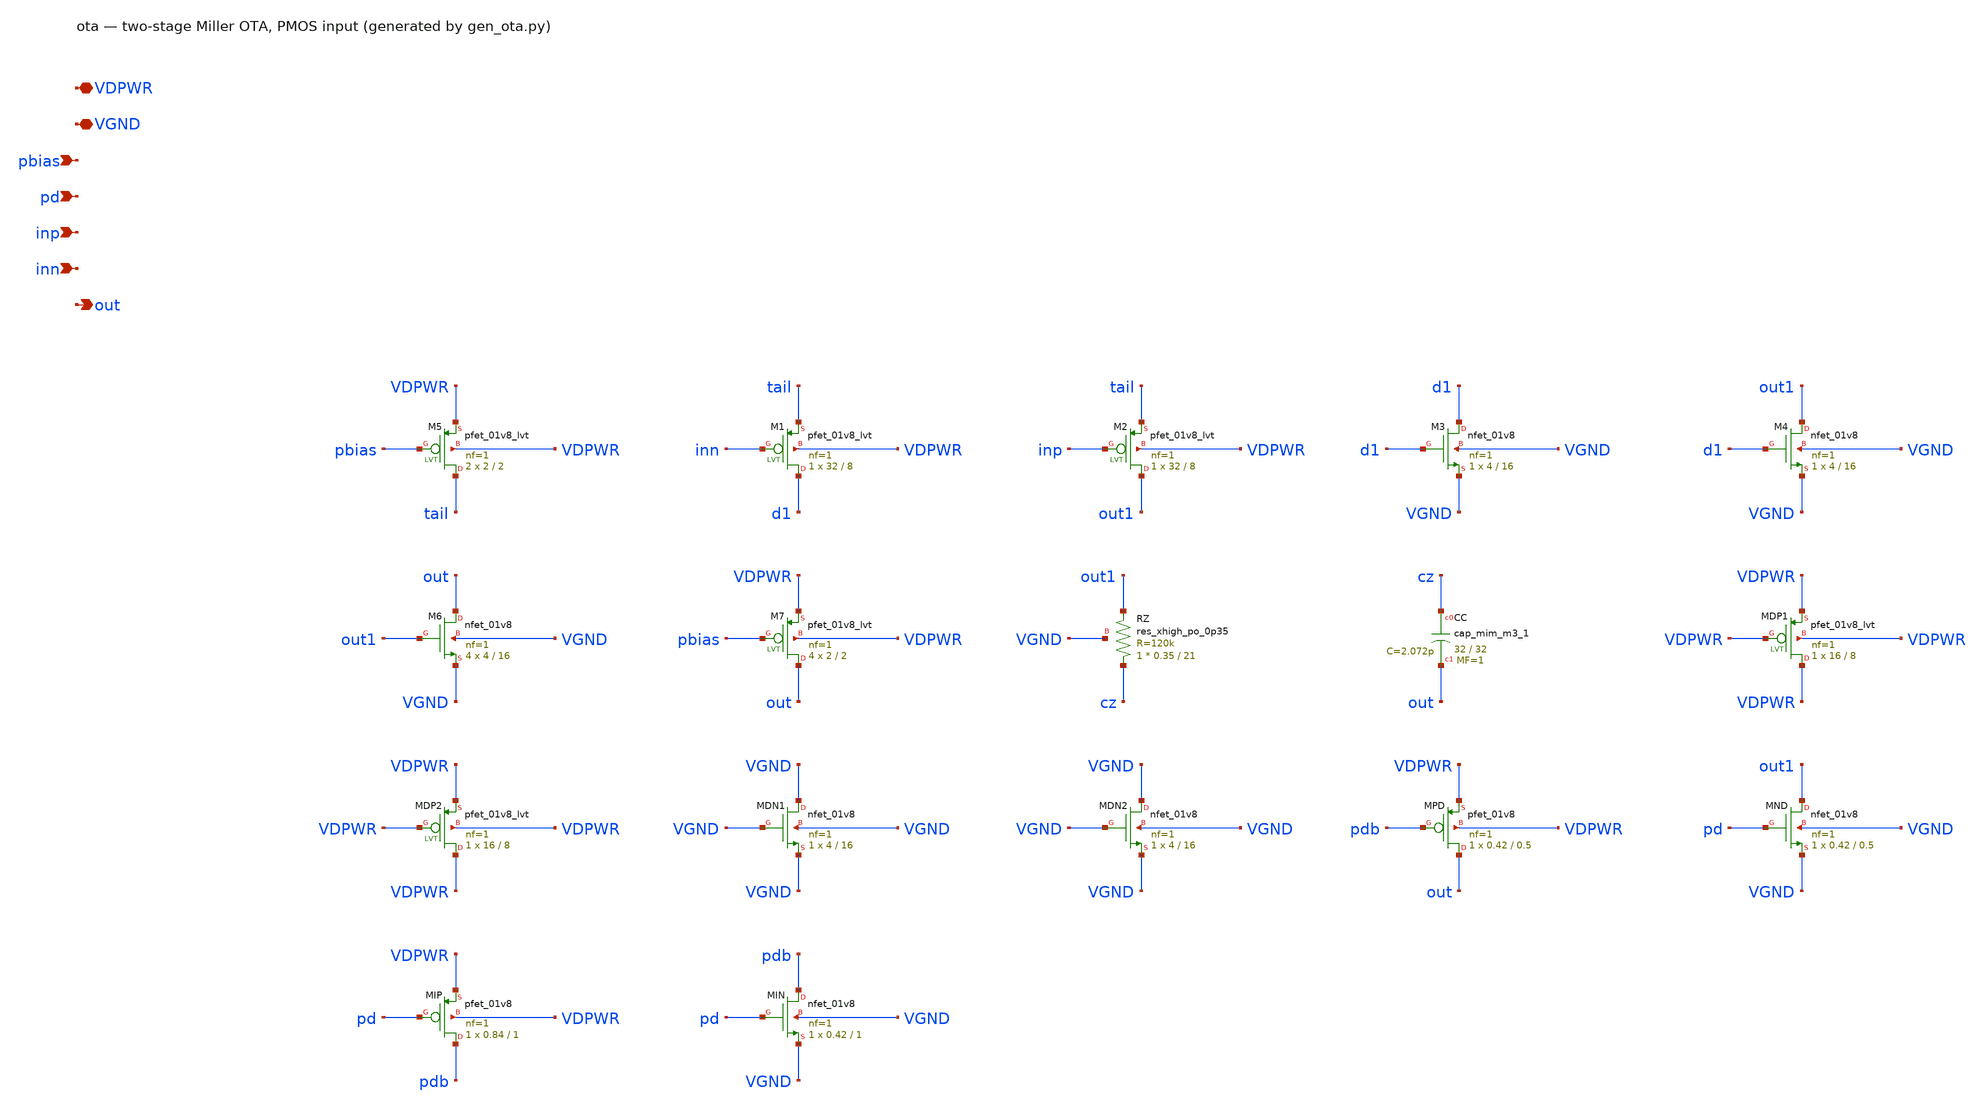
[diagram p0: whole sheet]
** sch_path: xschem/ota.sch
**.subckt ota VDPWR VGND pbias pd inp inn out
*.iopin VDPWR
*.iopin VGND
*.ipin pbias
*.ipin pd
*.ipin inp
*.ipin inn
*.opin out
XM5 tail pbias VDPWR VDPWR sky130_fd_pr__pfet_01v8_lvt L=2 W=2 nf=1 ad='int((1 + 1)/2) * 2 / 1 * 0.29'
+ as='int((1 + 2)/2) * 2 / 1 * 0.29' pd='2*int((1 + 1)/2) * (2 / 1 + 0.29)' ps='2*int((1 + 2)/2) * (2 / 1 + 0.29)'
+ nrd='0.29 / 2 ' nrs='0.29 / 2 ' sa=0 sb=0 sd=0 mult=2 m=2
XM1 d1 inn tail VDPWR sky130_fd_pr__pfet_01v8_lvt L=8 W=32 nf=1 ad='int((1 + 1)/2) * 32 / 1 * 0.29' as='int((1 + 2)/2) * 32 / 1 * 0.29'
+ pd='2*int((1 + 1)/2) * (32 / 1 + 0.29)' ps='2*int((1 + 2)/2) * (32 / 1 + 0.29)' nrd='0.29 / 32 ' nrs='0.29 / 32 '
+ sa=0 sb=0 sd=0 mult=1 m=1
XM2 out1 inp tail VDPWR sky130_fd_pr__pfet_01v8_lvt L=8 W=32 nf=1 ad='int((1 + 1)/2) * 32 / 1 * 0.29'
+ as='int((1 + 2)/2) * 32 / 1 * 0.29' pd='2*int((1 + 1)/2) * (32 / 1 + 0.29)' ps='2*int((1 + 2)/2) * (32 / 1 + 0.29)'
+ nrd='0.29 / 32 ' nrs='0.29 / 32 ' sa=0 sb=0 sd=0 mult=1 m=1
XM3 d1 d1 VGND VGND sky130_fd_pr__nfet_01v8 L=16 W=4 nf=1 ad='int((1 + 1)/2) * 4 / 1 * 0.29' as='int((1 + 2)/2) * 4 / 1 * 0.29'
+ pd='2*int((1 + 1)/2) * (4 / 1 + 0.29)' ps='2*int((1 + 2)/2) * (4 / 1 + 0.29)' nrd='0.29 / 4 ' nrs='0.29 / 4 '
+ sa=0 sb=0 sd=0 mult=1 m=1
XM4 out1 d1 VGND VGND sky130_fd_pr__nfet_01v8 L=16 W=4 nf=1 ad='int((1 + 1)/2) * 4 / 1 * 0.29' as='int((1 + 2)/2) * 4 / 1 * 0.29'
+ pd='2*int((1 + 1)/2) * (4 / 1 + 0.29)' ps='2*int((1 + 2)/2) * (4 / 1 + 0.29)' nrd='0.29 / 4 ' nrs='0.29 / 4 '
+ sa=0 sb=0 sd=0 mult=1 m=1
XM6 out out1 VGND VGND sky130_fd_pr__nfet_01v8 L=16 W=4 nf=1 ad='int((1 + 1)/2) * 4 / 1 * 0.29' as='int((1 + 2)/2) * 4 / 1 * 0.29'
+ pd='2*int((1 + 1)/2) * (4 / 1 + 0.29)' ps='2*int((1 + 2)/2) * (4 / 1 + 0.29)' nrd='0.29 / 4 ' nrs='0.29 / 4 '
+ sa=0 sb=0 sd=0 mult=4 m=4
XM7 out pbias VDPWR VDPWR sky130_fd_pr__pfet_01v8_lvt L=2 W=2 nf=1 ad='int((1 + 1)/2) * 2 / 1 * 0.29'
+ as='int((1 + 2)/2) * 2 / 1 * 0.29' pd='2*int((1 + 1)/2) * (2 / 1 + 0.29)' ps='2*int((1 + 2)/2) * (2 / 1 + 0.29)'
+ nrd='0.29 / 2 ' nrs='0.29 / 2 ' sa=0 sb=0 sd=0 mult=4 m=4
XRZ cz out1 VGND sky130_fd_pr__res_xhigh_po_0p35 L=21 mult=1 m=1
XCC cz out sky130_fd_pr__cap_mim_m3_1 W=32 L=32 MF=1 m=1
XMDP1 VDPWR VDPWR VDPWR VDPWR sky130_fd_pr__pfet_01v8_lvt L=8 W=16 nf=1 ad='int((1 + 1)/2) * 16 / 1 * 0.29'
+ as='int((1 + 2)/2) * 16 / 1 * 0.29' pd='2*int((1 + 1)/2) * (16 / 1 + 0.29)' ps='2*int((1 + 2)/2) * (16 / 1 + 0.29)'
+ nrd='0.29 / 16 ' nrs='0.29 / 16 ' sa=0 sb=0 sd=0 mult=1 m=1
XMDP2 VDPWR VDPWR VDPWR VDPWR sky130_fd_pr__pfet_01v8_lvt L=8 W=16 nf=1 ad='int((1 + 1)/2) * 16 / 1 * 0.29'
+ as='int((1 + 2)/2) * 16 / 1 * 0.29' pd='2*int((1 + 1)/2) * (16 / 1 + 0.29)' ps='2*int((1 + 2)/2) * (16 / 1 + 0.29)'
+ nrd='0.29 / 16 ' nrs='0.29 / 16 ' sa=0 sb=0 sd=0 mult=1 m=1
XMDN1 VGND VGND VGND VGND sky130_fd_pr__nfet_01v8 L=16 W=4 nf=1 ad='int((1 + 1)/2) * 4 / 1 * 0.29' as='int((1 + 2)/2) * 4 / 1 * 0.29'
+ pd='2*int((1 + 1)/2) * (4 / 1 + 0.29)' ps='2*int((1 + 2)/2) * (4 / 1 + 0.29)' nrd='0.29 / 4 ' nrs='0.29 / 4 '
+ sa=0 sb=0 sd=0 mult=1 m=1
XMDN2 VGND VGND VGND VGND sky130_fd_pr__nfet_01v8 L=16 W=4 nf=1 ad='int((1 + 1)/2) * 4 / 1 * 0.29' as='int((1 + 2)/2) * 4 / 1 * 0.29'
+ pd='2*int((1 + 1)/2) * (4 / 1 + 0.29)' ps='2*int((1 + 2)/2) * (4 / 1 + 0.29)' nrd='0.29 / 4 ' nrs='0.29 / 4 '
+ sa=0 sb=0 sd=0 mult=1 m=1
XMPD out pdb VDPWR VDPWR sky130_fd_pr__pfet_01v8 L=0.5 W=0.42 nf=1 ad='int((nf+1)/2) * W/nf * 0.29' as='int((nf+2)/2) * W/nf * 0.29'
+ pd='2*int((nf+1)/2) * (W/nf + 0.29)' ps='2*int((nf+2)/2) * (W/nf + 0.29)' nrd='0.29 / W' nrs='0.29 / W'
+ sa=0 sb=0 sd=0 mult=1 m=1
XMND out1 pd VGND VGND sky130_fd_pr__nfet_01v8 L=0.5 W=0.42 nf=1 ad='int((1 + 1)/2) * 0.42 / 1 * 0.29'
+ as='int((1 + 2)/2) * 0.42 / 1 * 0.29' pd='2*int((1 + 1)/2) * (0.42 / 1 + 0.29)' ps='2*int((1 + 2)/2) * (0.42 / 1 + 0.29)'
+ nrd='0.29 / 0.42 ' nrs='0.29 / 0.42 ' sa=0 sb=0 sd=0 mult=1 m=1
XMIP pdb pd VDPWR VDPWR sky130_fd_pr__pfet_01v8 L=1 W=0.84 nf=1 ad='int((nf+1)/2) * W/nf * 0.29' as='int((nf+2)/2) * W/nf * 0.29'
+ pd='2*int((nf+1)/2) * (W/nf + 0.29)' ps='2*int((nf+2)/2) * (W/nf + 0.29)' nrd='0.29 / W' nrs='0.29 / W'
+ sa=0 sb=0 sd=0 mult=1 m=1
XMIN pdb pd VGND VGND sky130_fd_pr__nfet_01v8 L=1 W=0.42 nf=1 ad='int((1 + 1)/2) * 0.42 / 1 * 0.29' as='int((1 + 2)/2) * 0.42 / 1 * 0.29'
+ pd='2*int((1 + 1)/2) * (0.42 / 1 + 0.29)' ps='2*int((1 + 2)/2) * (0.42 / 1 + 0.29)' nrd='0.29 / 0.42 '
+ nrs='0.29 / 0.42 ' sa=0 sb=0 sd=0 mult=1 m=1
**.ends
.end
